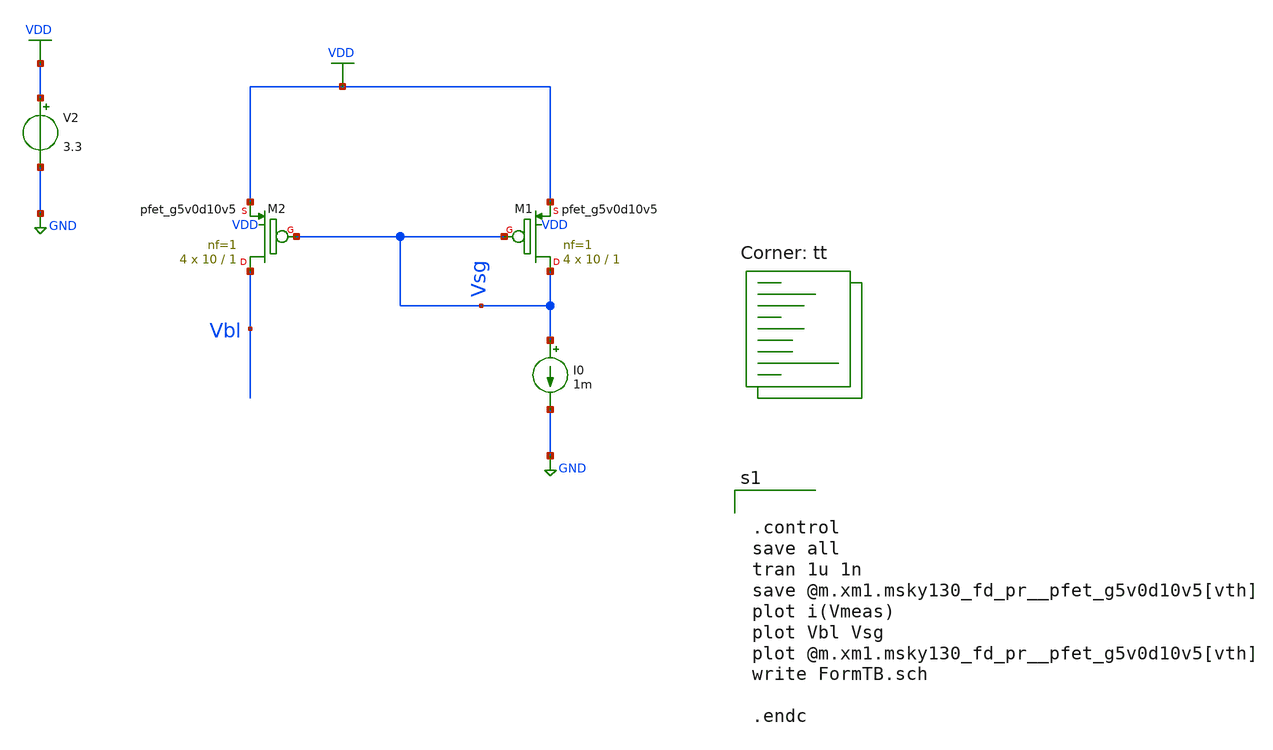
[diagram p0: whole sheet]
** sch_path: FormTB 1.sch
**.subckt FormTB 1
I0 Vsg GND 1m
V2 VDD GND 3.3
XM1 Vsg Vsg VDD VDD sky130_fd_pr__pfet_g5v0d10v5 L=1 W=10 nf=1 ad='int((nf+1)/2) * W/nf * 0.29' as='int((nf+2)/2) * W/nf * 0.29'
+ pd='2*int((nf+1)/2) * (W/nf + 0.29)' ps='2*int((nf+2)/2) * (W/nf + 0.29)' nrd='0.29 / W' nrs='0.29 / W'
+ sa=0 sb=0 sd=0 mult=4 m=4
XM2 Vbl Vsg VDD VDD sky130_fd_pr__pfet_g5v0d10v5 L=1 W=10 nf=1 ad='int((nf+1)/2) * W/nf * 0.29' as='int((nf+2)/2) * W/nf * 0.29'
+ pd='2*int((nf+1)/2) * (W/nf + 0.29)' ps='2*int((nf+2)/2) * (W/nf + 0.29)' nrd='0.29 / W' nrs='0.29 / W'
+ sa=0 sb=0 sd=0 mult=4 m=4
**** begin user architecture code
.lib $::SKYWATER_MODELS/sky130.lib.spice tt


.control
save all
tran 1u 1n
save @m.xm1.msky130_fd_pr__pfet_g5v0d10v5[vth]
plot i(Vmeas)
plot Vbl Vsg
plot @m.xm1.msky130_fd_pr__pfet_g5v0d10v5[vth]
write FormTB.sch

.endc


**** end user architecture code
**.ends
.GLOBAL GND
.GLOBAL VDD
.end
